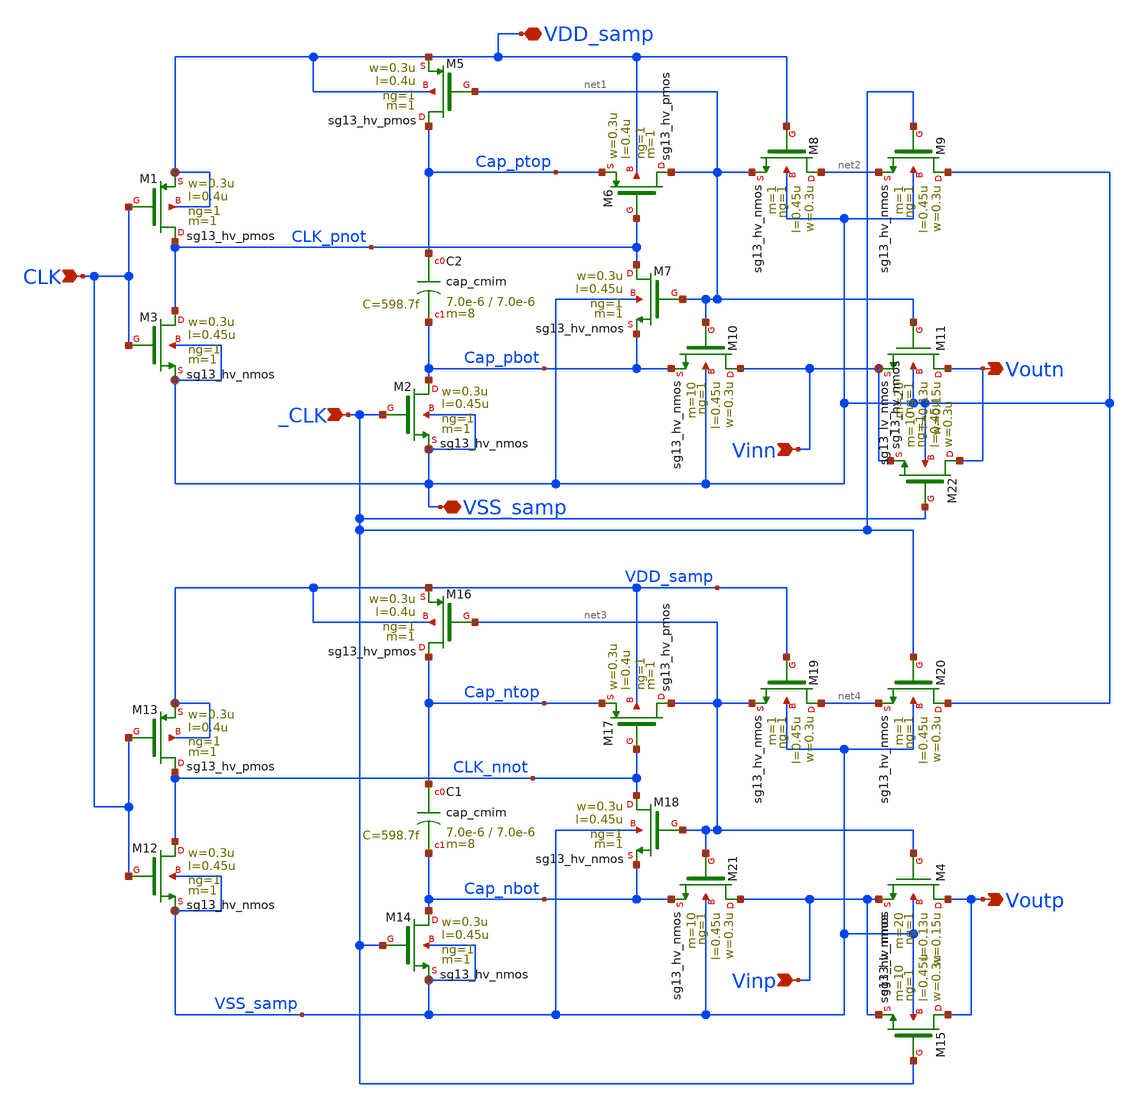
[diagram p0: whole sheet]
** sch_path: circuit_files/sar_adc_20260903/sampleAndHold.sch
**.subckt sampleAndHold CLK _CLK VDD_samp VSS_samp Vinn Voutn Vinp Voutp
*.ipin CLK
*.ipin _CLK
*.iopin VDD_samp
*.iopin VSS_samp
*.ipin Vinn
*.opin Voutn
*.ipin Vinp
*.opin Voutp
XM3 CLK_pnot CLK VSS_samp VSS_samp sg13_hv_nmos w=0.3u l=0.45u ng=1 m=1 mm_ok=1
XM1 CLK_pnot CLK VDD_samp VDD_samp sg13_hv_pmos w=0.3u l=0.4u ng=1 m=1 mm_ok=1
XM2 Cap_pbot _CLK VSS_samp VSS_samp sg13_hv_nmos w=0.3u l=0.45u ng=1 m=1 mm_ok=1
XM5 Cap_ptop net1 VDD_samp VDD_samp sg13_hv_pmos w=0.3u l=0.4u ng=1 m=1 mm_ok=1
XM6 net1 CLK_pnot Cap_ptop VDD_samp sg13_hv_pmos w=0.3u l=0.4u ng=1 m=1 mm_ok=1
XM7 CLK_pnot net1 Cap_pbot VSS_samp sg13_hv_nmos w=0.3u l=0.45u ng=1 m=1 mm_ok=1
XM8 net2 VDD_samp net1 VSS_samp sg13_hv_nmos w=0.3u l=0.45u ng=1 m=1 mm_ok=1
XM9 VSS_samp _CLK net2 VSS_samp sg13_hv_nmos w=0.3u l=0.45u ng=1 m=1 mm_ok=1
XM10 Vinn net1 Cap_pbot VSS_samp sg13_hv_nmos w=0.3u l=0.45u ng=1 m=10 mm_ok=1
XM12 CLK_nnot CLK VSS_samp VSS_samp sg13_hv_nmos w=0.3u l=0.45u ng=1 m=1 mm_ok=1
XM13 CLK_nnot CLK VDD_samp VDD_samp sg13_hv_pmos w=0.3u l=0.4u ng=1 m=1 mm_ok=1
XM14 Cap_nbot _CLK VSS_samp VSS_samp sg13_hv_nmos w=0.3u l=0.45u ng=1 m=1 mm_ok=1
XM16 Cap_ntop net3 VDD_samp VDD_samp sg13_hv_pmos w=0.3u l=0.4u ng=1 m=1 mm_ok=1
XM17 net3 CLK_nnot Cap_ntop VDD_samp sg13_hv_pmos w=0.3u l=0.4u ng=1 m=1 mm_ok=1
XM18 CLK_nnot net3 Cap_nbot VSS_samp sg13_hv_nmos w=0.3u l=0.45u ng=1 m=1 mm_ok=1
XM19 net4 VDD_samp net3 VSS_samp sg13_hv_nmos w=0.3u l=0.45u ng=1 m=1 mm_ok=1
XM20 VSS_samp _CLK net4 VSS_samp sg13_hv_nmos w=0.3u l=0.45u ng=1 m=1 mm_ok=1
XM21 Vinp net3 Cap_nbot VSS_samp sg13_hv_nmos w=0.3u l=0.45u ng=1 m=10 mm_ok=1
XC1 Cap_ntop Cap_nbot cap_cmim w=7.0e-6 l=7.0e-6 m=8 mm_ok=1
XC2 Cap_ptop Cap_pbot cap_cmim w=7.0e-6 l=7.0e-6 m=8 mm_ok=1
XM4 Voutp net3 Vinp VSS_samp sg13_lv_nmos w=0.15u l=0.13u ng=1 m=20 mm_ok=1
XM11 Voutn net1 Vinn VSS_samp sg13_lv_nmos w=0.15u l=0.13u ng=1 m=20 mm_ok=1
XM15 Voutp _CLK Vinp VSS_samp sg13_hv_nmos w=0.3u l=0.45u ng=1 m=10 mm_ok=1
XM22 Voutn _CLK Vinn VSS_samp sg13_hv_nmos w=0.3u l=0.45u ng=1 m=10 mm_ok=1
**.ends
.end
